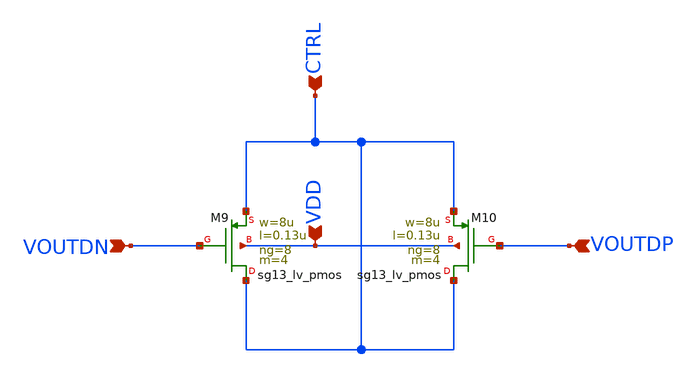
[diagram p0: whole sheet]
** sch_path: CDR4176-main/schematic/xschem/decap/decap.sch
**.subckt decap CTRL VDD VOUTDN VOUTDP
*.ipin CTRL
*.ipin VDD
*.ipin VOUTDN
*.ipin VOUTDP
XM10 CTRL VOUTDP CTRL VDD sg13_lv_pmos w=8u l=0.13u ng=8 m=4 mm_ok=1
XM9 CTRL VOUTDN CTRL VDD sg13_lv_pmos w=8u l=0.13u ng=8 m=4 mm_ok=1
**.ends
.end
